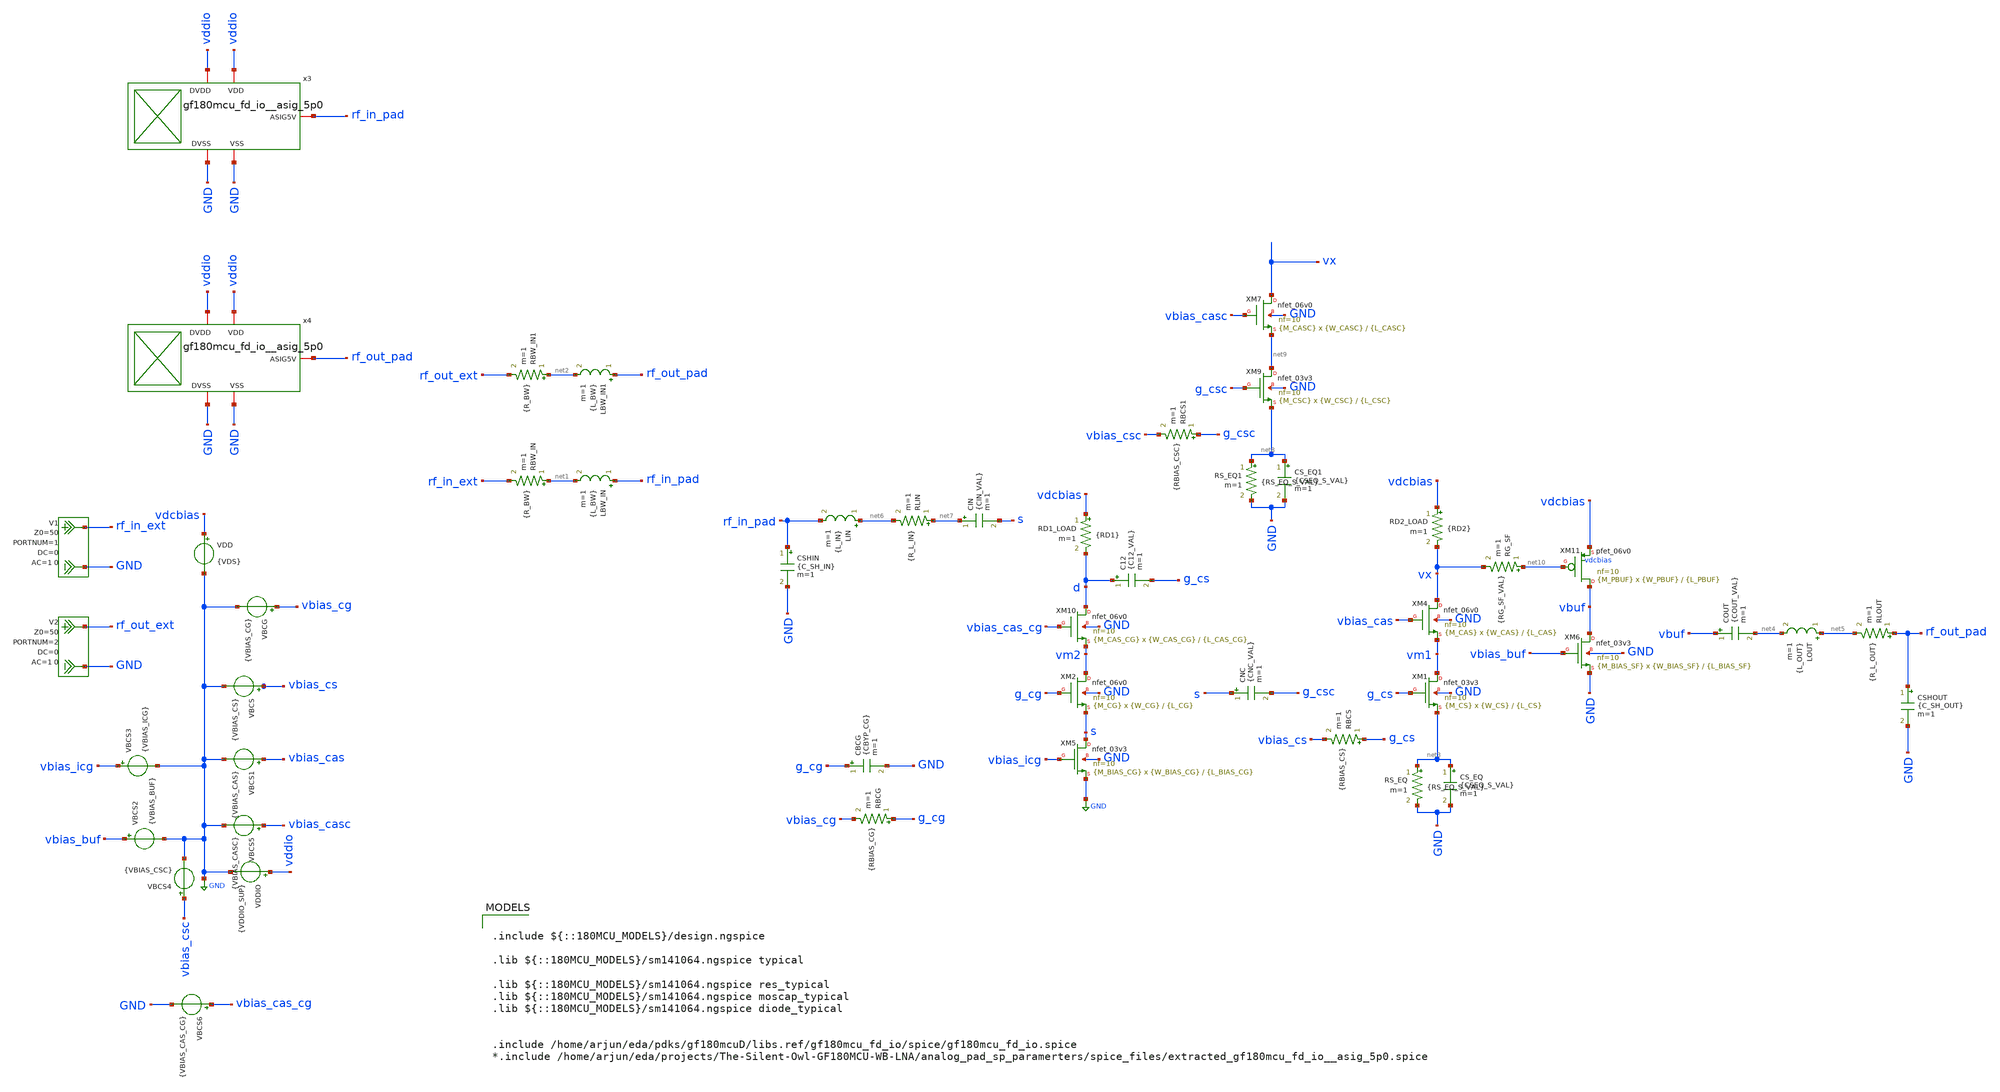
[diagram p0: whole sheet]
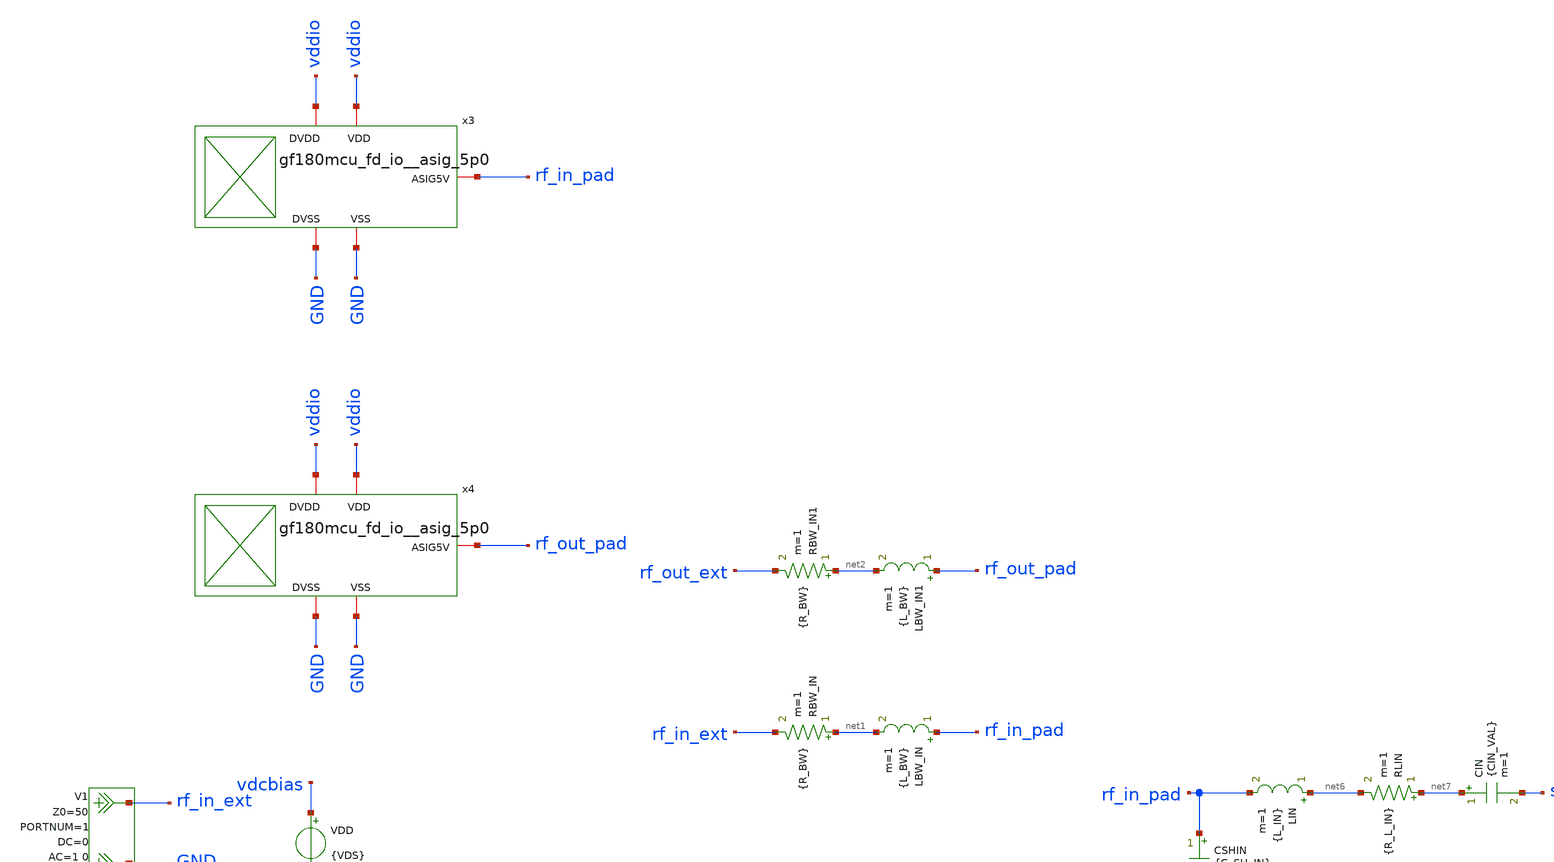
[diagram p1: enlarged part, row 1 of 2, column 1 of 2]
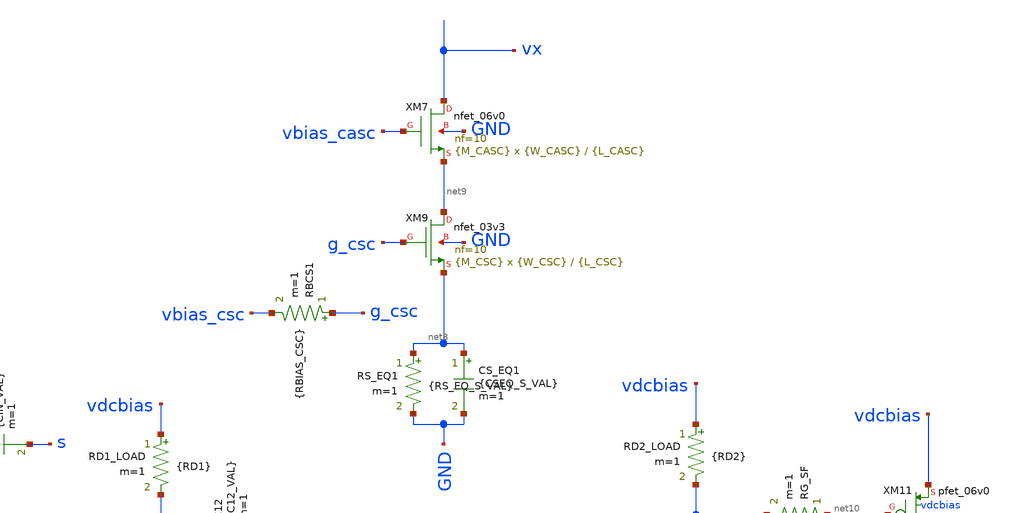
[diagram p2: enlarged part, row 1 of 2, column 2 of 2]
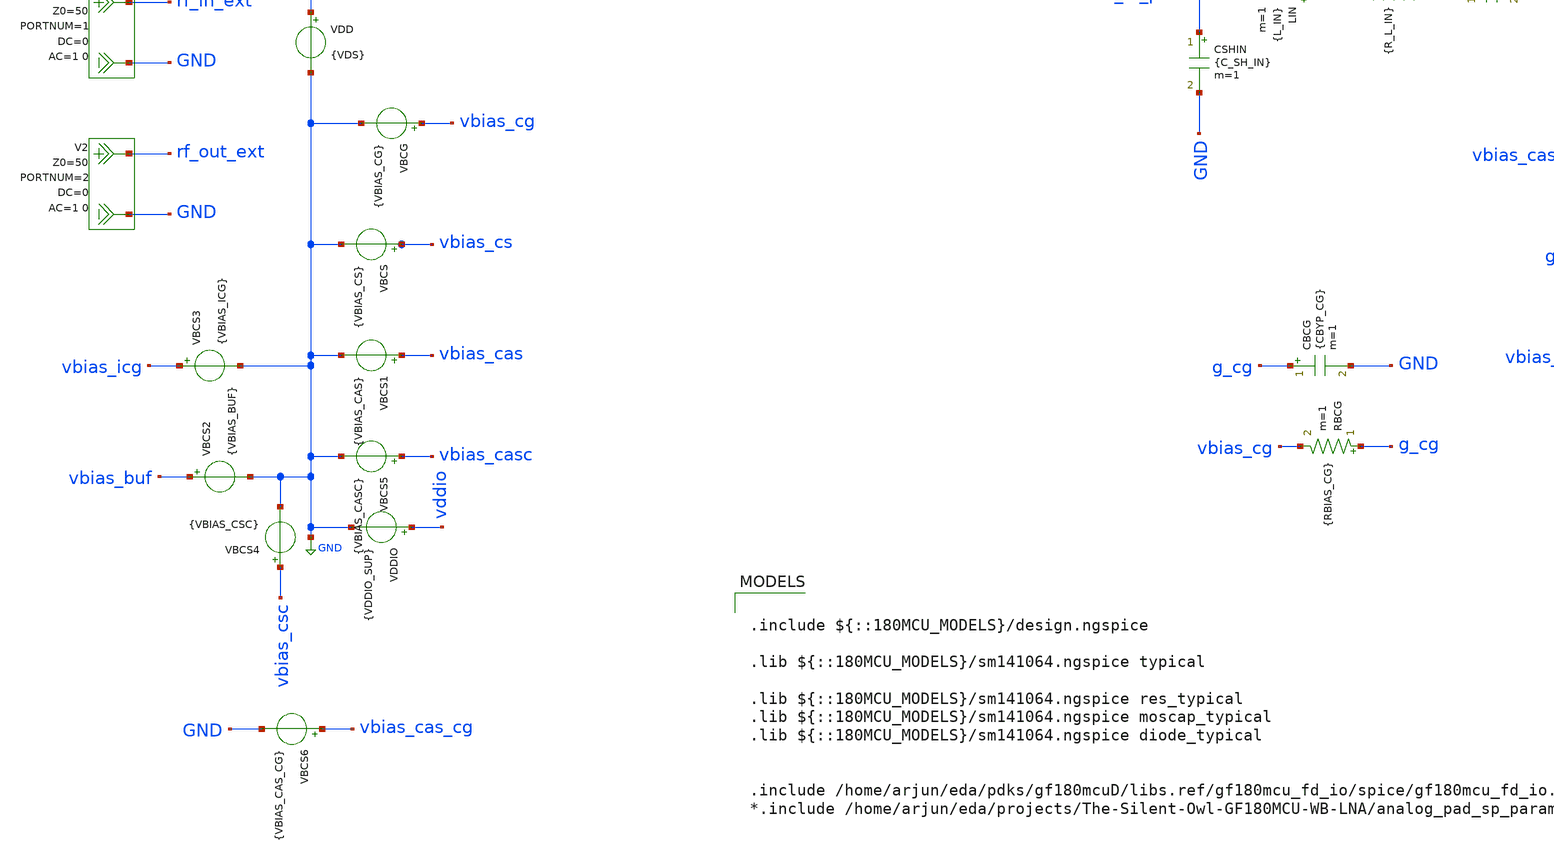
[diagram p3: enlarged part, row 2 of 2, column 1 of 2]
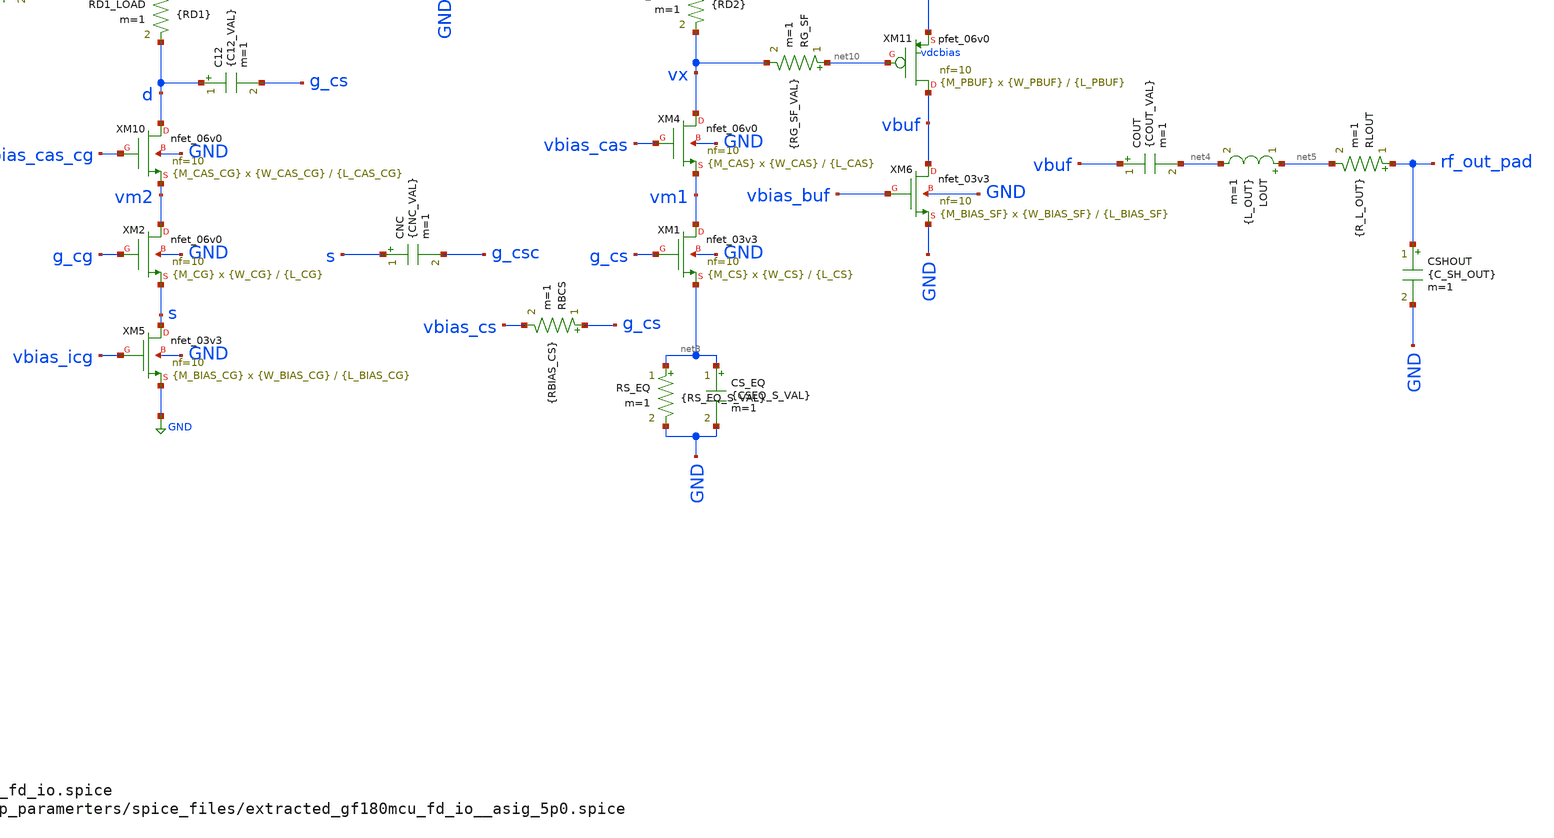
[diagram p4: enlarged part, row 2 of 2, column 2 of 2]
** sch_path: NFmin_Simulation/simulations/lna_core_06V_cgcs_sweep-2.sch
**.subckt lna_core_06V_cgcs_sweep-2
VBCG vbias_cg GND {VBIAS_CG}
VDD vdcbias GND {VDS}
C12 d g_cs {C12_VAL} m=1
CIN net7 s {CIN_VAL} m=1
V1 rf_in_ext GND DC 0 AC 1 0 portnum 1 z0 50
V2 rf_out_ext GND DC 0 AC 1 0 portnum 2 z0 50
XM2 vm2 g_cg s GND nfet_06v0 L={L_CG} W={W_CG} nf=10 ad='int((nf+1)/2) * W/nf * 0.18u' as='int((nf+2)/2) * W/nf * 0.18u'
+ pd='2*int((nf+1)/2) * (W/nf + 0.18u)' ps='2*int((nf+2)/2) * (W/nf + 0.18u)' nrd='0.18u / W' nrs='0.18u / W'
+ sa=0 sb=0 sd=0 m={M_CG}
RBCG g_cg vbias_cg {RBIAS_CG} m=1
CBCG g_cg GND {CBYP_CG} m=1
LBW_IN rf_in_pad net1 {L_BW} m=1
RBW_IN net1 rf_in_ext {R_BW} m=1
VDDIO vddio GND {VDDIO_SUP}
LBW_IN1 rf_out_pad net2 {L_BW} m=1
RBW_IN1 net2 rf_out_ext {R_BW} m=1
VBCS vbias_cs GND {VBIAS_CS}
RD1_LOAD vdcbias d {RD1} m=1
RBCS g_cs vbias_cs {RBIAS_CS} m=1
RD2_LOAD vdcbias vx {RD2} m=1
COUT vbuf net4 {COUT_VAL} m=1
LOUT net5 net4 {L_OUT} m=1
RLOUT rf_out_pad net5 {R_L_OUT} m=1
CSHOUT rf_out_pad GND {C_SH_OUT} m=1
CSHIN rf_in_pad GND {C_SH_IN} m=1
LIN net6 rf_in_pad {L_IN} m=1
RLIN net7 net6 {R_L_IN} m=1
XM4 vx vbias_cas vm1 GND nfet_06v0 L={L_CAS} W={W_CAS} nf=10 ad='int((nf+1)/2) * W/nf * 0.18u' as='int((nf+2)/2) * W/nf * 0.18u'
+ pd='2*int((nf+1)/2) * (W/nf + 0.18u)' ps='2*int((nf+2)/2) * (W/nf + 0.18u)' nrd='0.18u / W' nrs='0.18u / W'
+ sa=0 sb=0 sd=0 m={M_CAS}
VBCS1 vbias_cas GND {VBIAS_CAS}
VBCS2 vbias_buf GND {VBIAS_BUF}
VBCS3 vbias_icg GND {VBIAS_ICG}
XM5 s vbias_icg GND GND nfet_03v3 L={L_BIAS_CG} W={W_BIAS_CG} nf=10 ad='int((nf+1)/2) * W/nf * 0.18u'
+ as='int((nf+2)/2) * W/nf * 0.18u' pd='2*int((nf+1)/2) * (W/nf + 0.18u)' ps='2*int((nf+2)/2) * (W/nf + 0.18u)'
+ nrd='0.18u / W' nrs='0.18u / W' sa=0 sb=0 sd=0 m={M_BIAS_CG}
RS_EQ net3 GND {RS_EQ_S_VAL} m=1
CS_EQ net3 GND {CSEQ_S_VAL} m=1
XM1 vm1 g_cs net3 GND nfet_03v3 L={L_CS} W={W_CS} nf=10 ad='int((nf+1)/2) * W/nf * 0.18u' as='int((nf+2)/2) * W/nf * 0.18u'
+ pd='2*int((nf+1)/2) * (W/nf + 0.18u)' ps='2*int((nf+2)/2) * (W/nf + 0.18u)' nrd='0.18u / W' nrs='0.18u / W'
+ sa=0 sb=0 sd=0 m={M_CS}
RG_SF net10 vx {RG_SF_VAL} m=1
x3 rf_in_pad vddio GND vddio GND gf180mcu_fd_io__asig_5p0
x4 rf_out_pad vddio GND vddio GND gf180mcu_fd_io__asig_5p0
RBCS1 g_csc vbias_csc {RBIAS_CSC} m=1
XM7 vx vbias_casc net9 GND nfet_06v0 L={L_CASC} W={W_CASC} nf=10 ad='int((nf+1)/2) * W/nf * 0.18u' as='int((nf+2)/2) * W/nf * 0.18u'
+ pd='2*int((nf+1)/2) * (W/nf + 0.18u)' ps='2*int((nf+2)/2) * (W/nf + 0.18u)' nrd='0.18u / W' nrs='0.18u / W'
+ sa=0 sb=0 sd=0 m={M_CASC}
RS_EQ1 net8 GND {RS_EQ_S_VAL} m=1
CS_EQ1 net8 GND {CSEQ_S_VAL} m=1
XM9 net9 g_csc net8 GND nfet_03v3 L={L_CSC} W={W_CSC} nf=10 ad='int((nf+1)/2) * W/nf * 0.18u' as='int((nf+2)/2) * W/nf * 0.18u'
+ pd='2*int((nf+1)/2) * (W/nf + 0.18u)' ps='2*int((nf+2)/2) * (W/nf + 0.18u)' nrd='0.18u / W' nrs='0.18u / W'
+ sa=0 sb=0 sd=0 m={M_CSC}
VBCS4 vbias_csc GND {VBIAS_CSC}
VBCS5 vbias_casc GND {VBIAS_CASC}
CNC s g_csc {CNC_VAL} m=1
XM10 d vbias_cas_cg vm2 GND nfet_06v0 L={L_CAS_CG} W={W_CAS_CG} nf=10 ad='int((nf+1)/2) * W/nf * 0.18u'
+ as='int((nf+2)/2) * W/nf * 0.18u' pd='2*int((nf+1)/2) * (W/nf + 0.18u)' ps='2*int((nf+2)/2) * (W/nf + 0.18u)'
+ nrd='0.18u / W' nrs='0.18u / W' sa=0 sb=0 sd=0 m={M_CAS_CG}
VBCS6 vbias_cas_cg GND {VBIAS_CAS_CG}
XM11 vbuf net10 vdcbias vdcbias pfet_06v0 L={L_PBUF} W={W_PBUF} nf=10 ad='int((nf+1)/2) * W/nf * 0.18u'
+ as='int((nf+2)/2) * W/nf * 0.18u' pd='2*int((nf+1)/2) * (W/nf + 0.18u)' ps='2*int((nf+2)/2) * (W/nf + 0.18u)'
+ nrd='0.18u / W' nrs='0.18u / W' sa=0 sb=0 sd=0 m={M_PBUF} par={M_PBUF}
XM6 vbuf vbias_buf GND GND nfet_03v3 L={L_BIAS_SF} W={W_BIAS_SF} nf=10 ad='int((nf+1)/2) * W/nf * 0.18u'
+ as='int((nf+2)/2) * W/nf * 0.18u' pd='2*int((nf+1)/2) * (W/nf + 0.18u)' ps='2*int((nf+2)/2) * (W/nf + 0.18u)'
+ nrd='0.18u / W' nrs='0.18u / W' sa=0 sb=0 sd=0 m={M_BIAS_SF}
**** begin user architecture code

.include ${::180MCU_MODELS}/design.ngspice

.lib ${::180MCU_MODELS}/sm141064.ngspice typical

.lib ${::180MCU_MODELS}/sm141064.ngspice res_typical
.lib ${::180MCU_MODELS}/sm141064.ngspice moscap_typical
.lib ${::180MCU_MODELS}/sm141064.ngspice diode_typical


.include /home/arjun/eda/pdks/gf180mcuD/libs.ref/gf180mcu_fd_io/spice/gf180mcu_fd_io.spice
*.include /home/arjun/eda/projects/The-Silent-Owl-GF180MCU-WB-LNA/analog_pad_sp_paramerters/spice_files/extracted_gf180mcu_fd_io__asig_5p0.spice



.param VBIAS_CAS_CG=3.30
.param L_CAS_CG=0.60u
.param W_CAS_CG=80u
.param M_CAS_CG=4

.param L_PBUF=0.60u
.param W_PBUF=80u
.param M_PBUF=10

* Supply / package
.param VDS=5.0
.param VDDIO_SUP=5.0
.param L_BW=2n
.param R_BW=0.2

.param RS_EQ_D_VAL=8
.param CSEQ_D_VAL=8.2p
.param RS_EQ_S_VAL=8
.param CSEQ_S_VAL=8.2p

* Input network; legal intentional total = 2 nH
.param L_IN=1.80n
.param R_L_IN=2.26
.param CIN_VAL=100p
.param C_SH_IN=1f

* XM2 common-gate input
.param VBIAS_CG=2.05
.param W_CG=80u
.param M_CG=4
.param L_CG=0.60u
.param RD1=680
.param RBIAS_CG=50k
.param CBYP_CG=20p

* Mixed-voltage XM1/XM4 stage
.param C12_VAL=47p
.param VBIAS_CS=0.95
.param W_CS=40u
.param M_CS=2
.param L_CS=0.28u
.param RBIAS_CS=50k
.param VBIAS_CAS=3.30
.param W_CAS=70u
.param M_CAS=1
.param L_CAS=0.60u
.param RD2=250

* XM1 source equalizer
.param RS_EQ=8
.param CSEQ_VAL=8.2p

* Body-tied source follower and gate stopper
.param W_SF=50u
.param M_SF=5
.param L_SF=0.60u
.param RG_SF_VAL=0.25

* Output network
.param COUT_VAL=47p
.param L_OUT=0.20n
.param R_L_OUT=1.5
.param C_SH_OUT=1f

* XM5 common-gate current sink
.param VBIAS_ICG=1.65
.param L_BIAS_CG=0.50u
.param W_BIAS_CG=25u
.param M_BIAS_CG=1

* XM6 follower current sink
.param VBIAS_BUF=2.20
.param L_BIAS_SF=0.50u
.param W_BIAS_SF=50u
.param M_BIAS_SF=3


* Source-sensing common-source branch
.param RBIAS_CSC=50k
.param VBIAS_CSC=0.95
.param L_CSC=0.28u
.param W_CSC=10u
.param M_CSC=1

* Cancellation-branch cascode
.param VBIAS_CASC=3.30
.param L_CASC=0.60u
.param W_CASC=70u
.param M_CASC=1

.param CNC_VAL=47p






.control
set num_threads=6
option klu
set noaskquit
set wr_singlescale
set wr_vecnames
set numdgt=10

* =============================================================================
* GF180MCU LNA CORRECTED 10 mA HIGH-GAIN SWEEP
*
* IMPORTANT:
*   MOS widths and lengths remain unchanged.
*   Only multipliers, RD2 and VBIAS_BUF are swept.
*
* This sweep avoids the previous OP-to-SP inconsistency:
*
*   1. Apply candidate parameters.
*   2. Run OP.
*   3. Save all DC values.
*   4. Keep the OP plot alive.
*   5. Run SP for the same candidate.
*   6. Save RF results.
*   7. Destroy both plots.
*
* Search strategy:
*
*   RD2:
*       Controls the PMOS gate-driving operating point.
*
*   M_PBUF:
*       Kept substantially smaller than the previous M=56-88 search
*       whenever RD2 can provide stronger PMOS overdrive.
*
*   M_BIAS_SF and VBIAS_BUF:
*       Restore approximately 10 mA and VBUF near 2.5 V.
*
* Approximate DC search size:
*
*   17 RD2 values
*   14 PMOS multiplier values
*   21 NMOS multiplier values
*   13 bias values
*
*   Total = 64,974 operating points
*
* RF simulation runs only for DC-valid points.
* =============================================================================


* =============================================================================
* DESIGN TARGETS
* =============================================================================

let target_current=10e-3
let target_vbuf=2.50
let target_gain=20.0

* Enforce a substantially tighter 10 mA window.
let min_current=9.0e-3
let max_current=11.0e-3

let min_gmp=20e-3
let min_gmn=20e-3

let min_satp=0.20
let min_satn=0.20

let max_current_error=2.0

let target_s11=-10.0
let target_s22=-10.0
let target_nf=5.0

let target_mu=1.05
let target_mup=1.05


* =============================================================================
* OUTPUT FILES
* =============================================================================

echo ============================================================ > lna_10ma_corrected_sweep.txt
echo GF180MCU_LNA_CORRECTED_10MA_HIGH_GAIN_SWEEP >> lna_10ma_corrected_sweep.txt
echo ============================================================ >> lna_10ma_corrected_sweep.txt
echo MOS_WIDTHS_AND_LENGTHS_FIXED >> lna_10ma_corrected_sweep.txt
echo PRIMARY_SELECTION_METRIC_MAXIMUM_S21_AT_2P4_GHZ >> lna_10ma_corrected_sweep.txt
echo CURRENT_WINDOW_A_0P009_TO_0P011 >> lna_10ma_corrected_sweep.txt
echo ============================================================ >> lna_10ma_corrected_sweep.txt
echo COLUMNS RD2_OHM M_PBUF M_BIAS_SF VBIAS_BUF_V VBUF_V IP_A IN_A CURRENT_ERROR_PERCENT GMP_S GMN_S
+ GMIDP_1_PER_V GMIDN_1_PER_V PMOS_SAT_MARGIN_V NMOS_SAT_MARGIN_V S11_DB S21_DB S12_DB S22_DB NF_DB NFMIN_DB K MU
+ MUP DELTA_MAG VALID SCORE >> lna_10ma_corrected_sweep.txt
echo ============================================================ >> lna_10ma_corrected_sweep.txt

echo ============================================================ > lna_10ma_corrected_summary.txt
echo GF180MCU_LNA_CORRECTED_10MA_SELECTED_DESIGN >> lna_10ma_corrected_summary.txt
echo ============================================================ >> lna_10ma_corrected_summary.txt
echo MOS_WIDTHS_AND_LENGTHS_FIXED_TO_SCHEMATIC_VALUES >> lna_10ma_corrected_summary.txt
echo ============================================================ >> lna_10ma_corrected_summary.txt


* =============================================================================
* INITIALIZE SEARCH STATISTICS
* =============================================================================

set found=0
set total_points=0
set dc_valid_points=0
set stable_rf_points=0
set gain20_points=0

set best_score=1e99

set best_rd2=450
set best_mp=68
set best_mn=34
set best_vbn=0.870

set best_vbuf=0

set best_ip=0
set best_in=0
set best_ierr=0

set best_gmp=0
set best_gmn=0
set best_gmidp=0
set best_gmidn=0

set best_satp=0
set best_satn=0

set best_s11=0
set best_s21=-1e99
set best_s12=0
set best_s22=0

set best_nf=0
set best_nfmin=0

set best_k=0
set best_mu=0
set best_mup=0
set best_delta=0


* =============================================================================
* SUPER-LARGE ACTIVE-PARAMETER SWEEP
*
* RD2:
*   440 to 520 ohm, step 5 ohm
*
* M_PBUF:
*   4 to 56, step 4
*
* M_BIAS_SF:
*   16 to 96, step 4
*
* VBIAS_BUF:
*   0.75 to 1.05 V, step 0.025 V
* =============================================================================

let rd2v=440

while rd2v <= 520

    let mp=4

    while mp <= 56

        let mn=16

        while mn <= 96

            let vbn=0.750

            while vbn <= 1.050001

                let count_tmp=$total_points+1
                set total_points=$&count_tmp

                * =============================================================
                * APPLY THIS CANDIDATE
                * =============================================================

                alterparam RD2=$&rd2v
                alterparam M_PBUF=$&mp
                alterparam M_BIAS_SF=$&mn

                reset

                alter VBCS2=$&vbn


                * =============================================================
                * DC OPERATING POINT
                * =============================================================

                op

                set opplot=$curplot

                let vb=v(vbuf)

                * -------------------------------------------------------------
                * XM11 PMOS
                * -------------------------------------------------------------

                let ip=abs(@m.xm11.m0[id])
                let gmp=abs(@m.xm11.m0[gm])

                let vsdp=abs(@m.xm11.m0[vds])
                let vdsatp=abs(@m.xm11.m0[vdsat])
                let satp=vsdp-vdsatp

                let gmidp=gmp/(ip+1e-30)

                * -------------------------------------------------------------
                * XM6 NMOS
                * -------------------------------------------------------------

                let in=abs(@m.xm6.m0[id])
                let gmn=abs(@m.xm6.m0[gm])

                let vdsn=@m.xm6.m0[vds]
                let vdsatn=abs(@m.xm6.m0[vdsat])
                let satn=vdsn-vdsatn

                let gmidn=gmn/(in+1e-30)

                let ierr=100*abs(ip-in)/(0.5*(ip+in)+1e-30)


                * =============================================================
                * NAN-SAFE DC VALIDITY
                * =============================================================

                let dcvalid=0

                if vb > 2.00
                    if vb < 3.00
                        if ip > min_current
                            if ip < max_current
                                if in > min_current
                                    if in < max_current
                                        if gmp > min_gmp
                                            if gmn > min_gmn
                                                if ierr < max_current_error
                                                    if satp > min_satp
                                                        if satn > min_satn
                                                            let dcvalid=1
                                                        end
                                                    end
                                                end
                                            end
                                        end
                                    end
                                end
                            end
                        end
                    end
                end


                * =============================================================
                * SAVE DC VALUES BEFORE STARTING SP
                *
                * These shell variables remain available after SP changes the
                * current plot.
                * =============================================================

                set cand_vbuf=$&vb

                set cand_ip=$&ip
                set cand_in=$&in
                set cand_ierr=$&ierr

                set cand_gmp=$&gmp
                set cand_gmn=$&gmn

                set cand_gmidp=$&gmidp
                set cand_gmidn=$&gmidn

                set cand_satp=$&satp
                set cand_satn=$&satn


                * =============================================================
                * RUN RF ONLY FOR A VALID 10 mA OPERATING POINT
                * =============================================================

                if dcvalid = 1

                    let dc_count_tmp=$dc_valid_points+1
                    set dc_valid_points=$&dc_count_tmp

                    * ---------------------------------------------------------
                    * Do not destroy the OP plot here.
                    *
                    * SP therefore evaluates the same altered candidate.
                    *
                    * Three points:
                    *   index 0 = 2.399 GHz
                    *   index 1 = 2.400 GHz
                    *   index 2 = 2.401 GHz
                    * ---------------------------------------------------------

                    sp lin 3 2.399Gig 2.401Gig 1

                    set spplot=$curplot

                    let s11db=db(s_1_1)
                    let s21db=db(s_2_1)
                    let s12db=db(s_1_2)
                    let s22db=db(s_2_2)

                    let nfdb=real(NF)
                    let nfmindb=real(NFmin)

                    let delta=s_1_1*s_2_2-s_1_2*s_2_1
                    let deltamag=mag(delta)

                    let a11=mag(s_1_1)
                    let a12=mag(s_1_2)
                    let a21=mag(s_2_1)
                    let a22=mag(s_2_2)

                    let kval=(1-a11*a11-a22*a22+deltamag*deltamag)/(2*a12*a21+1e-30)

                    let mu=(1-a11*a11)/(mag(s_2_2-delta*conj(s_1_1))+mag(s_1_2*s_2_1)+1e-30)

                    let mup=(1-a22*a22)/(mag(s_1_1-delta*conj(s_2_2))+mag(s_1_2*s_2_1)+1e-30)

                    let s11c=s11db[1]
                    let s21c=s21db[1]
                    let s12c=s12db[1]
                    let s22c=s22db[1]

                    let nfc=nfdb[1]
                    let nfminc=nfmindb[1]

                    let kc=kval[1]
                    let muc=mu[1]
                    let mupc=mup[1]
                    let deltac=deltamag[1]


                    * =========================================================
                    * STABILITY VALIDITY
                    * =========================================================

                    let rfvalid=0

                    if kc > 1.0
                        if muc > 1.0
                            if mupc > 1.0
                                if deltac < 1.0
                                    let rfvalid=1
                                end
                            end
                        end
                    end


                    * =========================================================
                    * DIAGNOSTIC SCORE
                    *
                    * Actual winner is chosen primarily by maximum S21.
                    *
                    * The score is included to show penalties for:
                    *   current error
                    *   VBUF error
                    *   NF
                    *   return losses
                    *   large PMOS multiplier
                    * =========================================================

                    let score=1e99

                    if rfvalid = 1

                        let stable_count_tmp=$stable_rf_points+1
                        set stable_rf_points=$&stable_count_tmp

                        let score=-100*s21c

                        let score=score+5000*abs($cand_ip-target_current)
                        let score=score+5000*abs($cand_in-target_current)

                        let score=score+10*abs($cand_vbuf-target_vbuf)
                        let score=score+0.20*$cand_ierr

                        let score=score+2*nfc

                        * Mild preference for smaller PMOS multiplier.
                        let score=score+0.05*mp

                        if s21c < target_gain
                            let score=score+100*(target_gain-s21c)
                        end

                        if s11c > target_s11
                            let score=score+5*(s11c-target_s11)
                        end

                        if s22c > target_s22
                            let score=score+5*(s22c-target_s22)
                        end

                        if nfc > target_nf
                            let score=score+2*(nfc-target_nf)
                        end

                        if muc < target_mu
                            let score=score+100*(target_mu-muc)
                        end

                        if mupc < target_mup
                            let score=score+100*(target_mup-mupc)
                        end

                        if s21c > target_gain
                            let gain_count_tmp=$gain20_points+1
                            set gain20_points=$&gain_count_tmp
                        end

                    end


                    * =========================================================
                    * WRITE COMPLETE SAME-CANDIDATE DC AND RF DATA
                    * =========================================================

                    echo $&rd2v $&mp $&mn $&vbn $cand_vbuf $cand_ip $cand_in $cand_ierr $cand_gmp
+ $cand_gmn $cand_gmidp $cand_gmidn $cand_satp $cand_satn $&s11c $&s21c $&s12c $&s22c $&nfc $&nfminc $&kc $&muc
+ $&mupc $&deltac $&rfvalid $&score >> lna_10ma_corrected_sweep.txt


                    * =========================================================
                    * SELECT MAXIMUM-S21 VALID POINT
                    * =========================================================

                    if rfvalid = 1

                        if $found = 0

                            set found=1

                            set best_score=$&score

                            set best_rd2=$&rd2v
                            set best_mp=$&mp
                            set best_mn=$&mn
                            set best_vbn=$&vbn

                            set best_vbuf=$cand_vbuf

                            set best_ip=$cand_ip
                            set best_in=$cand_in
                            set best_ierr=$cand_ierr

                            set best_gmp=$cand_gmp
                            set best_gmn=$cand_gmn

                            set best_gmidp=$cand_gmidp
                            set best_gmidn=$cand_gmidn

                            set best_satp=$cand_satp
                            set best_satn=$cand_satn

                            set best_s11=$&s11c
                            set best_s21=$&s21c
                            set best_s12=$&s12c
                            set best_s22=$&s22c

                            set best_nf=$&nfc
                            set best_nfmin=$&nfminc

                            set best_k=$&kc
                            set best_mu=$&muc
                            set best_mup=$&mupc
                            set best_delta=$&deltac

                        else

                            if s21c > $best_s21

                                set best_score=$&score

                                set best_rd2=$&rd2v
                                set best_mp=$&mp
                                set best_mn=$&mn
                                set best_vbn=$&vbn

                                set best_vbuf=$cand_vbuf

                                set best_ip=$cand_ip
                                set best_in=$cand_in
                                set best_ierr=$cand_ierr

                                set best_gmp=$cand_gmp
                                set best_gmn=$cand_gmn

                                set best_gmidp=$cand_gmidp
                                set best_gmidn=$cand_gmidn

                                set best_satp=$cand_satp
                                set best_satn=$cand_satn

                                set best_s11=$&s11c
                                set best_s21=$&s21c
                                set best_s12=$&s12c
                                set best_s22=$&s22c

                                set best_nf=$&nfc
                                set best_nfmin=$&nfminc

                                set best_k=$&kc
                                set best_mu=$&muc
                                set best_mup=$&mupc
                                set best_delta=$&deltac

                            end

                        end

                    end


                    * =========================================================
                    * DESTROY BOTH PLOTS ONLY AFTER DATA HAS BEEN SAVED
                    * =========================================================

                    destroy $spplot
                    destroy $opplot

                else

                    echo $&rd2v $&mp $&mn $&vbn $cand_vbuf $cand_ip $cand_in $cand_ierr $cand_gmp
+ $cand_gmn $cand_gmidp $cand_gmidn $cand_satp $cand_satn 0 -1E+99 0 0 0 0 0 0 0 0 0 1E+99 >>
+ lna_10ma_corrected_sweep.txt

                    destroy $opplot

                end

                let vbn=vbn+0.025

            end

            let mn=mn+4

        end

        let mp=mp+4

    end

    let rd2v=rd2v+5

end


* =============================================================================
* SWEEP SUMMARY
* =============================================================================

echo ============================================================ >> lna_10ma_corrected_sweep.txt
echo CORRECTED_SWEEP_SUMMARY >> lna_10ma_corrected_sweep.txt

echo TOTAL_POINTS $total_points >> lna_10ma_corrected_sweep.txt
echo DC_VALID_9_TO_11MA_POINTS $dc_valid_points >> lna_10ma_corrected_sweep.txt
echo STABLE_RF_POINTS $stable_rf_points >> lna_10ma_corrected_sweep.txt
echo S21_ABOVE_20DB_POINTS $gain20_points >> lna_10ma_corrected_sweep.txt

echo BEST_FOUND $found >> lna_10ma_corrected_sweep.txt

echo BEST_RD2_OHM $best_rd2 >> lna_10ma_corrected_sweep.txt
echo BEST_M_PBUF $best_mp >> lna_10ma_corrected_sweep.txt
echo BEST_M_BIAS_SF $best_mn >> lna_10ma_corrected_sweep.txt
echo BEST_VBIAS_BUF_V $best_vbn >> lna_10ma_corrected_sweep.txt

echo BEST_VBUF_V $best_vbuf >> lna_10ma_corrected_sweep.txt

echo BEST_PMOS_CURRENT_A $best_ip >> lna_10ma_corrected_sweep.txt
echo BEST_NMOS_CURRENT_A $best_in >> lna_10ma_corrected_sweep.txt
echo BEST_CURRENT_ERROR_PERCENT $best_ierr >> lna_10ma_corrected_sweep.txt

echo BEST_PMOS_GM_S $best_gmp >> lna_10ma_corrected_sweep.txt
echo BEST_NMOS_GM_S $best_gmn >> lna_10ma_corrected_sweep.txt
echo BEST_PMOS_GMID_1_PER_V $best_gmidp >> lna_10ma_corrected_sweep.txt
echo BEST_NMOS_GMID_1_PER_V $best_gmidn >> lna_10ma_corrected_sweep.txt

echo BEST_PMOS_SATURATION_MARGIN_V $best_satp >> lna_10ma_corrected_sweep.txt
echo BEST_NMOS_SATURATION_MARGIN_V $best_satn >> lna_10ma_corrected_sweep.txt

echo BEST_S11_DB $best_s11 >> lna_10ma_corrected_sweep.txt
echo BEST_S21_DB $best_s21 >> lna_10ma_corrected_sweep.txt
echo BEST_S12_DB $best_s12 >> lna_10ma_corrected_sweep.txt
echo BEST_S22_DB $best_s22 >> lna_10ma_corrected_sweep.txt

echo BEST_NF_DB $best_nf >> lna_10ma_corrected_sweep.txt
echo BEST_NFMIN_DB $best_nfmin >> lna_10ma_corrected_sweep.txt

echo BEST_K $best_k >> lna_10ma_corrected_sweep.txt
echo BEST_MU $best_mu >> lna_10ma_corrected_sweep.txt
echo BEST_MUP $best_mup >> lna_10ma_corrected_sweep.txt
echo BEST_DELTA_MAG $best_delta >> lna_10ma_corrected_sweep.txt

echo BEST_SCORE $best_score >> lna_10ma_corrected_sweep.txt
echo ============================================================ >> lna_10ma_corrected_sweep.txt


* =============================================================================
* FINAL VERIFICATION OF THE ACTUAL BEST POINT
* =============================================================================

if $found = 1

    alterparam RD2=$best_rd2
    alterparam M_PBUF=$best_mp
    alterparam M_BIAS_SF=$best_mn

    reset

    alter VBCS2=$best_vbn


    * =========================================================================
    * FINAL DC OPERATING POINT
    * =========================================================================

    op

    let final_vbuf=v(vbuf)

    let final_ip=abs(@m.xm11.m0[id])
    let final_gmp=abs(@m.xm11.m0[gm])
    let final_vsgp=abs(@m.xm11.m0[vgs])
    let final_vsdp=abs(@m.xm11.m0[vds])
    let final_vdsatp=abs(@m.xm11.m0[vdsat])
    let final_satp=final_vsdp-final_vdsatp
    let final_gmidp=final_gmp/(final_ip+1e-30)

    let final_in=abs(@m.xm6.m0[id])
    let final_gmn=abs(@m.xm6.m0[gm])
    let final_vgsn=@m.xm6.m0[vgs]
    let final_vdsn=@m.xm6.m0[vds]
    let final_vdsatn=abs(@m.xm6.m0[vdsat])
    let final_satn=final_vdsn-final_vdsatn
    let final_gmidn=final_gmn/(final_in+1e-30)

    let final_ierr=100*abs(final_ip-final_in)/(0.5*(final_ip+final_in)+1e-30)
    let final_gmerr=100*abs(final_gmp-final_gmn)/(0.5*(final_gmp+final_gmn)+1e-30)

    let final_power=1000*5*final_ip

    set final_vbuf_saved=$&final_vbuf

    set final_ip_saved=$&final_ip
    set final_in_saved=$&final_in
    set final_ierr_saved=$&final_ierr

    set final_gmp_saved=$&final_gmp
    set final_gmn_saved=$&final_gmn
    set final_gmerr_saved=$&final_gmerr

    set final_gmidp_saved=$&final_gmidp
    set final_gmidn_saved=$&final_gmidn

    set final_vsgp_saved=$&final_vsgp
    set final_vsdp_saved=$&final_vsdp
    set final_vdsatp_saved=$&final_vdsatp
    set final_satp_saved=$&final_satp

    set final_vgsn_saved=$&final_vgsn
    set final_vdsn_saved=$&final_vdsn
    set final_vdsatn_saved=$&final_vdsatn
    set final_satn_saved=$&final_satn

    set final_power_saved=$&final_power

    destroy $curplot


    * =========================================================================
    * FINAL TARGET BAND
    * =========================================================================

    alterparam RD2=$best_rd2
    alterparam M_PBUF=$best_mp
    alterparam M_BIAS_SF=$best_mn

    reset

    alter VBCS2=$best_vbn

    sp lin 101 2.30Gig 2.50Gig 1

    set targetplot=$curplot

    let fghz=frequency/1e9

    let s11db=db(s_1_1)
    let s21db=db(s_2_1)
    let s12db=db(s_1_2)
    let s22db=db(s_2_2)

    let nfdb=real(NF)
    let nfmindb=real(NFmin)

    let delta=s_1_1*s_2_2-s_1_2*s_2_1
    let deltamag=mag(delta)

    let a11=mag(s_1_1)
    let a12=mag(s_1_2)
    let a21=mag(s_2_1)
    let a22=mag(s_2_2)

    let kval=(1-a11*a11-a22*a22+deltamag*deltamag)/(2*a12*a21+1e-30)

    let mu=(1-a11*a11)/(mag(s_2_2-delta*conj(s_1_1))+mag(s_1_2*s_2_1)+1e-30)

    let mup=(1-a22*a22)/(mag(s_1_1-delta*conj(s_2_2))+mag(s_1_2*s_2_1)+1e-30)

    let zin=50*(1+s_1_1)/(1-s_1_1)
    let zout=50*(1+s_2_2)/(1-s_2_2)

    let zinre=real(zin)
    let zinim=imag(zin)

    let zoutre=real(zout)
    let zoutim=imag(zout)

    let s11worst=s11db[0]
    let s21min=s21db[0]
    let s21max=s21db[0]
    let s22worst=s22db[0]

    let nfworst=nfdb[0]
    let nfminworst=nfmindb[0]

    let kmin=kval[0]
    let mumin=mu[0]
    let mupmin=mup[0]
    let deltamax=deltamag[0]

    let ii=1

    while ii < 101

        if s11db[ii] > s11worst
            let s11worst=s11db[ii]
        end

        if s21db[ii] < s21min
            let s21min=s21db[ii]
        end

        if s21db[ii] > s21max
            let s21max=s21db[ii]
        end

        if s22db[ii] > s22worst
            let s22worst=s22db[ii]
        end

        if nfdb[ii] > nfworst
            let nfworst=nfdb[ii]
        end

        if nfmindb[ii] > nfminworst
            let nfminworst=nfmindb[ii]
        end

        if kval[ii] < kmin
            let kmin=kval[ii]
        end

        if mu[ii] < mumin
            let mumin=mu[ii]
        end

        if mup[ii] < mupmin
            let mupmin=mup[ii]
        end

        if deltamag[ii] > deltamax
            let deltamax=deltamag[ii]
        end

        let ii=ii+1

    end

    let ripple=s21max-s21min

    let center_frequency=frequency[50]

    let center_s11=s11db[50]
    let center_s21=s21db[50]
    let center_s12=s12db[50]
    let center_s22=s22db[50]

    let center_nf=nfdb[50]
    let center_nfmin=nfmindb[50]

    let center_k=kval[50]
    let center_mu=mu[50]
    let center_mup=mup[50]
    let center_delta=deltamag[50]

    let center_zinre=zinre[50]
    let center_zinim=zinim[50]

    let center_zoutre=zoutre[50]
    let center_zoutim=zoutim[50]

    wrdata lna_10ma_corrected_target_band.txt frequency s11db s21db s12db s22db nfdb nfmindb kval mu
+ mup deltamag zinre zinim zoutre zoutim


    * =========================================================================
    * FINAL SUMMARY FILE
    * =========================================================================

    echo SELECTED_PARAMETERS >> lna_10ma_corrected_summary.txt

    echo RD2_OHM $best_rd2 >> lna_10ma_corrected_summary.txt
    echo M_PBUF $best_mp >> lna_10ma_corrected_summary.txt
    echo M_BIAS_SF $best_mn >> lna_10ma_corrected_summary.txt
    echo VBIAS_BUF_V $best_vbn >> lna_10ma_corrected_summary.txt

    echo ============================================================ >>
+ lna_10ma_corrected_summary.txt
    echo DC_OPERATING_POINT >> lna_10ma_corrected_summary.txt

    echo VBUF_V $final_vbuf_saved >> lna_10ma_corrected_summary.txt

    echo PMOS_CURRENT_A $final_ip_saved >> lna_10ma_corrected_summary.txt
    echo NMOS_CURRENT_A $final_in_saved >> lna_10ma_corrected_summary.txt
    echo CURRENT_ERROR_PERCENT $final_ierr_saved >> lna_10ma_corrected_summary.txt

    echo PMOS_GM_S $final_gmp_saved >> lna_10ma_corrected_summary.txt
    echo NMOS_GM_S $final_gmn_saved >> lna_10ma_corrected_summary.txt
    echo GM_ERROR_PERCENT $final_gmerr_saved >> lna_10ma_corrected_summary.txt

    echo PMOS_GMID_1_PER_V $final_gmidp_saved >> lna_10ma_corrected_summary.txt
    echo NMOS_GMID_1_PER_V $final_gmidn_saved >> lna_10ma_corrected_summary.txt

    echo PMOS_VSG_V $final_vsgp_saved >> lna_10ma_corrected_summary.txt
    echo PMOS_VSD_V $final_vsdp_saved >> lna_10ma_corrected_summary.txt
    echo PMOS_VDSAT_V $final_vdsatp_saved >> lna_10ma_corrected_summary.txt
    echo PMOS_SATURATION_MARGIN_V $final_satp_saved >> lna_10ma_corrected_summary.txt

    echo NMOS_VGS_V $final_vgsn_saved >> lna_10ma_corrected_summary.txt
    echo NMOS_VDS_V $final_vdsn_saved >> lna_10ma_corrected_summary.txt
    echo NMOS_VDSAT_V $final_vdsatn_saved >> lna_10ma_corrected_summary.txt
    echo NMOS_SATURATION_MARGIN_V $final_satn_saved >> lna_10ma_corrected_summary.txt

    echo BUFFER_BRANCH_POWER_MW $final_power_saved >> lna_10ma_corrected_summary.txt

    echo ============================================================ >>
+ lna_10ma_corrected_summary.txt
    echo TARGET_BAND_2P30_TO_2P50_GHZ >> lna_10ma_corrected_summary.txt

    echo S11_WORST_DB $&s11worst >> lna_10ma_corrected_summary.txt
    echo S21_MIN_DB $&s21min >> lna_10ma_corrected_summary.txt
    echo S21_MAX_DB $&s21max >> lna_10ma_corrected_summary.txt
    echo GAIN_RIPPLE_DB $&ripple >> lna_10ma_corrected_summary.txt
    echo S22_WORST_DB $&s22worst >> lna_10ma_corrected_summary.txt

    echo NF_WORST_DB $&nfworst >> lna_10ma_corrected_summary.txt
    echo NFMIN_WORST_DB $&nfminworst >> lna_10ma_corrected_summary.txt

    echo K_MIN $&kmin >> lna_10ma_corrected_summary.txt
    echo MU_MIN $&mumin >> lna_10ma_corrected_summary.txt
    echo MUP_MIN $&mupmin >> lna_10ma_corrected_summary.txt
    echo DELTA_MAX $&deltamax >> lna_10ma_corrected_summary.txt

    echo ============================================================ >>
+ lna_10ma_corrected_summary.txt
    echo RESULTS_AT_2P4_GHZ >> lna_10ma_corrected_summary.txt

    echo ACTUAL_FREQUENCY_HZ $&center_frequency >> lna_10ma_corrected_summary.txt

    echo S11_DB $&center_s11 >> lna_10ma_corrected_summary.txt
    echo S21_DB $&center_s21 >> lna_10ma_corrected_summary.txt
    echo S12_DB $&center_s12 >> lna_10ma_corrected_summary.txt
    echo S22_DB $&center_s22 >> lna_10ma_corrected_summary.txt

    echo NF_DB $&center_nf >> lna_10ma_corrected_summary.txt
    echo NFMIN_DB $&center_nfmin >> lna_10ma_corrected_summary.txt

    echo K $&center_k >> lna_10ma_corrected_summary.txt
    echo MU $&center_mu >> lna_10ma_corrected_summary.txt
    echo MUP $&center_mup >> lna_10ma_corrected_summary.txt
    echo DELTA_MAG $&center_delta >> lna_10ma_corrected_summary.txt

    echo ZIN_REAL_OHM $&center_zinre >> lna_10ma_corrected_summary.txt
    echo ZIN_IMAG_OHM $&center_zinim >> lna_10ma_corrected_summary.txt

    echo ZOUT_REAL_OHM $&center_zoutre >> lna_10ma_corrected_summary.txt
    echo ZOUT_IMAG_OHM $&center_zoutim >> lna_10ma_corrected_summary.txt

    echo ============================================================ >>
+ lna_10ma_corrected_summary.txt

    destroy $curplot


    * =========================================================================
    * BROADBAND VERIFICATION
    * =========================================================================

    alterparam RD2=$best_rd2
    alterparam M_PBUF=$best_mp
    alterparam M_BIAS_SF=$best_mn

    reset

    alter VBCS2=$best_vbn

    sp lin 7000 1Meg 7Gig 1

    set broadbandplot=$curplot

    let fghz=frequency/1e9

    let s11db=db(s_1_1)
    let s21db=db(s_2_1)
    let s12db=db(s_1_2)
    let s22db=db(s_2_2)

    let nfdb=real(NF)
    let nfmindb=real(NFmin)

    let delta=s_1_1*s_2_2-s_1_2*s_2_1
    let deltamag=mag(delta)

    let a11=mag(s_1_1)
    let a12=mag(s_1_2)
    let a21=mag(s_2_1)
    let a22=mag(s_2_2)

    let kval=(1-a11*a11-a22*a22+deltamag*deltamag)/(2*a12*a21+1e-30)

    let mu=(1-a11*a11)/(mag(s_2_2-delta*conj(s_1_1))+mag(s_1_2*s_2_1)+1e-30)

    let mup=(1-a22*a22)/(mag(s_1_1-delta*conj(s_2_2))+mag(s_1_2*s_2_1)+1e-30)

    let zin=50*(1+s_1_1)/(1-s_1_1)
    let zout=50*(1+s_2_2)/(1-s_2_2)

    let zinre=real(zin)
    let zinim=imag(zin)

    let zoutre=real(zout)
    let zoutim=imag(zout)

    wrdata lna_10ma_corrected_broadband.txt frequency s11db s21db s12db s22db nfdb nfmindb kval mu
+ mup deltamag zinre zinim zoutre zoutim

    echo GENERATED_FILES >> lna_10ma_corrected_summary.txt
    echo SWEEP_FILE lna_10ma_corrected_sweep.txt >> lna_10ma_corrected_summary.txt
    echo SUMMARY_FILE lna_10ma_corrected_summary.txt >> lna_10ma_corrected_summary.txt
    echo TARGET_BAND_FILE lna_10ma_corrected_target_band.txt >> lna_10ma_corrected_summary.txt
    echo BROADBAND_FILE lna_10ma_corrected_broadband.txt >> lna_10ma_corrected_summary.txt
    echo ============================================================ >>
+ lna_10ma_corrected_summary.txt


    * =========================================================================
    * PLOTS
    * =========================================================================

    setplot $targetplot
    setscale fghz

    plot s11db xlimit 2.3 2.5
    plot s21db xlimit 2.3 2.5
    plot s22db xlimit 2.3 2.5
    plot nfdb nfmindb xlimit 2.3 2.5
    plot mu mup xlimit 2.3 2.5

    setplot $broadbandplot
    setscale fghz

    plot s11db s21db s22db xlimit 0 7
    plot mu mup xlimit 0 7

    echo ============================================================
    echo CORRECTED_10MA_HIGH_GAIN_SWEEP_COMPLETE
    echo TOTAL_POINTS_$total_points
    echo DC_VALID_POINTS_$dc_valid_points
    echo STABLE_RF_POINTS_$stable_rf_points
    echo S21_ABOVE_20DB_POINTS_$gain20_points
    echo BEST_S21_DB_$best_s21
    echo SUMMARY_lna_10ma_corrected_summary.txt
    echo ============================================================

else

    echo ============================================================
    echo ERROR_NO_STABLE_9_TO_11MA_POINT_FOUND
    echo CHECK_lna_10ma_corrected_sweep.txt
    echo ============================================================

end

.endc


**** end user architecture code
**.ends
.GLOBAL GND
.end
